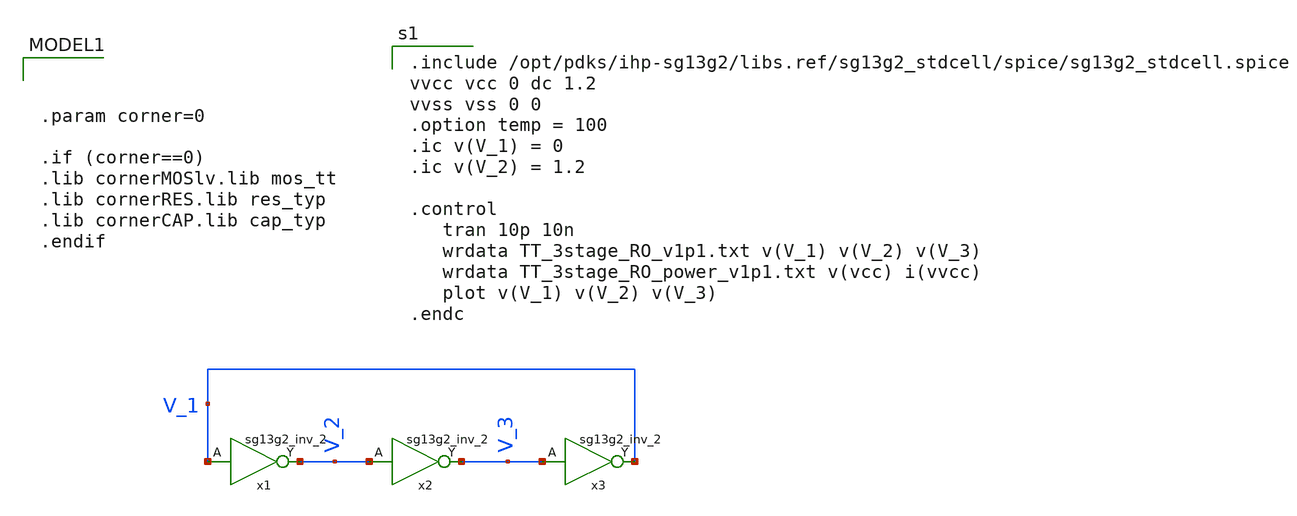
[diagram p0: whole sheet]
** sch_path: Day1/tb_3stage_RO.sch
* IHP-GmbH/IHP-Open-PDK/ihp-sg13g2/libs.tech/xschem/sg13g2_stdcells/sg13g2_inv_2.sch:
* Copyright 2023 IHP PDK Authors
* Licensed under the Apache License, Version 2.0 (the "License");
**.subckt tb_3stage_RO
x1 V_2 V_1 VCC VSS sg13g2_inv_2
x2 V_3 V_2 VCC VSS sg13g2_inv_2
x3 V_1 V_3 VCC VSS sg13g2_inv_2
**** begin user architecture code

.include /opt/pdks/ihp-sg13g2/libs.ref/sg13g2_stdcell/spice/sg13g2_stdcell.spice
vvcc vcc 0 dc 1.2
vvss vss 0 0
.option temp = 100
.ic v(V_1) = 0
.ic v(V_2) = 1.2

.control
   tran 10p 10n
   wrdata TT_3stage_RO_v1p1.txt v(V_1) v(V_2) v(V_3)
   wrdata TT_3stage_RO_power_v1p1.txt v(vcc) i(vvcc)
   plot v(V_1) v(V_2) v(V_3)
.endc




.param corner=0

.if (corner==0)
.lib cornerMOSlv.lib mos_tt
.lib cornerRES.lib res_typ
.lib cornerCAP.lib cap_typ
.endif

**** end user architecture code
**.ends

* expanding   symbol:  sg13g2_inv_2.sym # of pins=2
** sym_path: sg13g2_inv_2.sym
** sch_path: sg13g2_inv_2.sch
.subckt sg13g2_inv_2 Y A VDD VSS
*.opin Y
*.ipin A
*.iopin VDD
*.iopin VSS
XM1 Y A VSS VSS sg13_lv_nmos w=1.48u l=130.00n ng=2 m=1 mm_ok=1
XM2 Y A VDD VDD sg13_lv_pmos w=2.24u l=130.00n ng=2 m=1 mm_ok=1
.ends

.end
